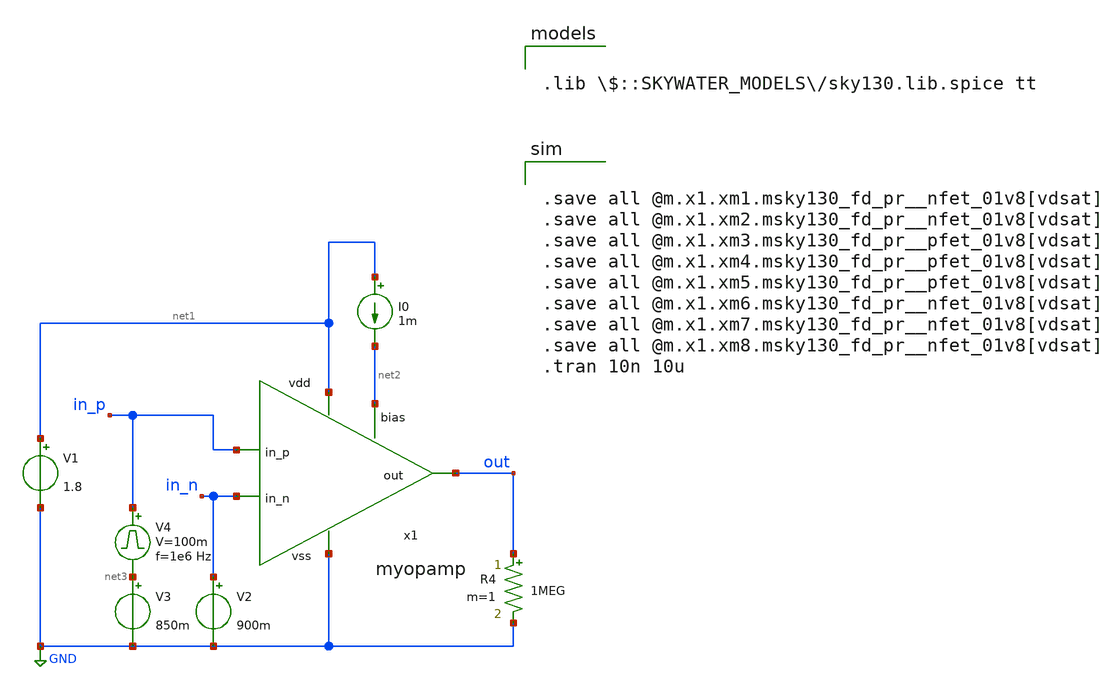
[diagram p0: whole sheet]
** sch_path: design/myopamp/test/tb.sch
**.subckt tb
x1 net1 in_n in_p out net2 GND myopamp
V1 net1 GND 1.8
I0 net1 net2 1m
R4 out GND 1MEG m=1
V2 in_n GND 900m
V3 net3 GND 850m
V4 in_p net3 pulse 0 100m '0.495/ 1e6 ' '0.01/1e6 ' '0.01/1e6 ' '0.49/1e6 ' '1/1e6 '
**** begin user architecture code


.save all @m.x1.xm1.msky130_fd_pr__nfet_01v8[vdsat]
.save all @m.x1.xm2.msky130_fd_pr__nfet_01v8[vdsat]
.save all @m.x1.xm3.msky130_fd_pr__pfet_01v8[vdsat]
.save all @m.x1.xm4.msky130_fd_pr__pfet_01v8[vdsat]
.save all @m.x1.xm5.msky130_fd_pr__pfet_01v8[vdsat]
.save all @m.x1.xm6.msky130_fd_pr__nfet_01v8[vdsat]
.save all @m.x1.xm7.msky130_fd_pr__nfet_01v8[vdsat]
.save all @m.x1.xm8.msky130_fd_pr__nfet_01v8[vdsat]
.tran 10n 10u



.lib $::SKYWATER_MODELS/sky130.lib.spice tt

**** end user architecture code
**.ends

* expanding   symbol:  myopamp/myopamp.sym # of pins=6
** sym_path: design/myopamp/myopamp.sym
** sch_path: design/myopamp/myopamp.sch
.subckt myopamp vdd in_n in_p out bias vss
*.ipin in_n
*.ipin in_p
*.ipin bias
*.opin out
*.iopin vdd
*.iopin vss
XM1 net2 in_n net1 vss sky130_fd_pr__nfet_01v8 L=0.15 W=1 nf=1 ad='int((nf+1)/2) * W/nf * 0.29' as='int((nf+2)/2) * W/nf * 0.29'
+ pd='2*int((nf+1)/2) * (W/nf + 0.29)' ps='2*int((nf+2)/2) * (W/nf + 0.29)' nrd='0.29 / W' nrs='0.29 / W'
+ sa=0 sb=0 sd=0 mult=1 m=1
XM2 net3 in_p net1 vss sky130_fd_pr__nfet_01v8 L=0.15 W=1 nf=1 ad='int((nf+1)/2) * W/nf * 0.29' as='int((nf+2)/2) * W/nf * 0.29'
+ pd='2*int((nf+1)/2) * (W/nf + 0.29)' ps='2*int((nf+2)/2) * (W/nf + 0.29)' nrd='0.29 / W' nrs='0.29 / W'
+ sa=0 sb=0 sd=0 mult=1 m=1
XM3 vdd net2 net2 vdd sky130_fd_pr__pfet_01v8 L=0.35 W=1 nf=1 ad='int((nf+1)/2) * W/nf * 0.29' as='int((nf+2)/2) * W/nf * 0.29'
+ pd='2*int((nf+1)/2) * (W/nf + 0.29)' ps='2*int((nf+2)/2) * (W/nf + 0.29)' nrd='0.29 / W' nrs='0.29 / W'
+ sa=0 sb=0 sd=0 mult=1 m=1
XM4 vdd net2 net3 vdd sky130_fd_pr__pfet_01v8 L=0.35 W=1 nf=1 ad='int((nf+1)/2) * W/nf * 0.29' as='int((nf+2)/2) * W/nf * 0.29'
+ pd='2*int((nf+1)/2) * (W/nf + 0.29)' ps='2*int((nf+2)/2) * (W/nf + 0.29)' nrd='0.29 / W' nrs='0.29 / W'
+ sa=0 sb=0 sd=0 mult=1 m=1
XM5 vdd net3 out vdd sky130_fd_pr__pfet_01v8 L=0.35 W=1 nf=1 ad='int((nf+1)/2) * W/nf * 0.29' as='int((nf+2)/2) * W/nf * 0.29'
+ pd='2*int((nf+1)/2) * (W/nf + 0.29)' ps='2*int((nf+2)/2) * (W/nf + 0.29)' nrd='0.29 / W' nrs='0.29 / W'
+ sa=0 sb=0 sd=0 mult=1 m=1
XM6 bias bias vss vss sky130_fd_pr__nfet_01v8 L=0.15 W=1 nf=1 ad='int((nf+1)/2) * W/nf * 0.29' as='int((nf+2)/2) * W/nf * 0.29'
+ pd='2*int((nf+1)/2) * (W/nf + 0.29)' ps='2*int((nf+2)/2) * (W/nf + 0.29)' nrd='0.29 / W' nrs='0.29 / W'
+ sa=0 sb=0 sd=0 mult=1 m=1
XM7 net1 bias vss vss sky130_fd_pr__nfet_01v8 L=0.15 W=1 nf=1 ad='int((nf+1)/2) * W/nf * 0.29' as='int((nf+2)/2) * W/nf * 0.29'
+ pd='2*int((nf+1)/2) * (W/nf + 0.29)' ps='2*int((nf+2)/2) * (W/nf + 0.29)' nrd='0.29 / W' nrs='0.29 / W'
+ sa=0 sb=0 sd=0 mult=1 m=1
XM8 out bias vss vss sky130_fd_pr__nfet_01v8 L=0.15 W=1 nf=1 ad='int((nf+1)/2) * W/nf * 0.29' as='int((nf+2)/2) * W/nf * 0.29'
+ pd='2*int((nf+1)/2) * (W/nf + 0.29)' ps='2*int((nf+2)/2) * (W/nf + 0.29)' nrd='0.29 / W' nrs='0.29 / W'
+ sa=0 sb=0 sd=0 mult=1 m=1
.ends

.GLOBAL GND
.end
